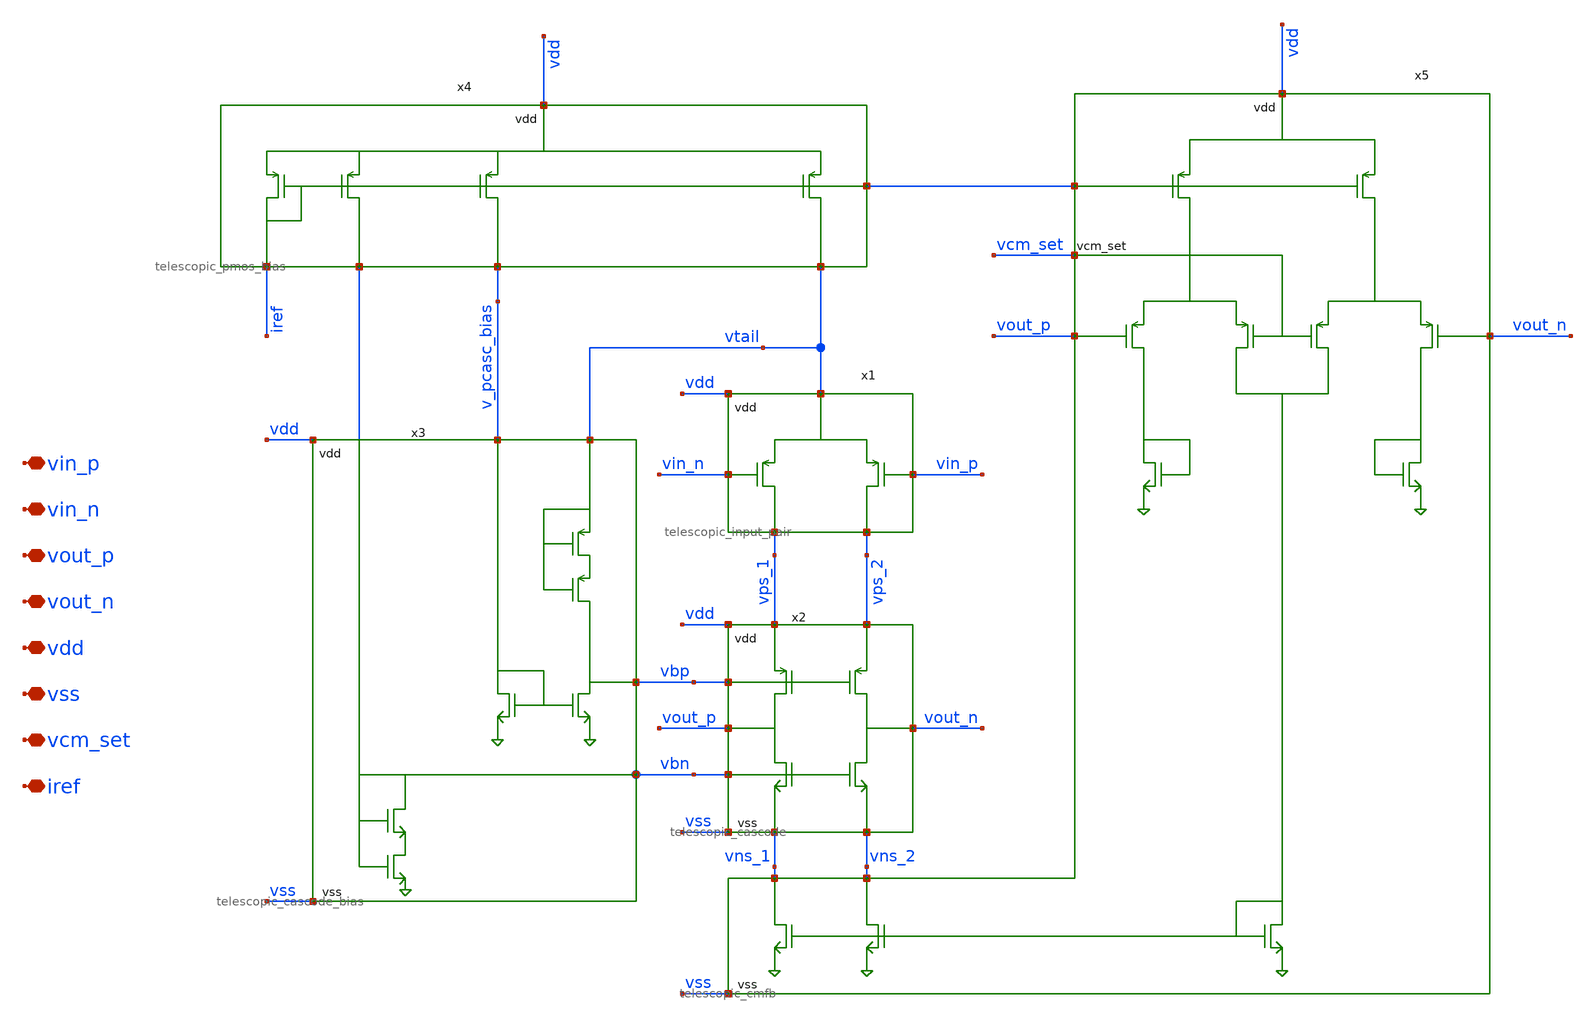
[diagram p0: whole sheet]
** sch_path: xschem/archive/rrl/telescopic.sch
**.subckt telescopic vin_p vin_n vout_p vout_n vdd vss vcm_set iref
*.iopin vin_p
*.iopin vin_n
*.iopin vout_p
*.iopin vout_n
*.iopin vdd
*.iopin vss
*.iopin vcm_set
*.iopin iref
x1 vtail vdd vin_n vin_p vps_1 vps_2 telescopic_input_pair
x2 vdd vss vps_1 vps_2 vns_1 vns_2 vout_p vout_n vbp vbn telescopic_cascode
x3 vbn v_pcasc_bias vtail vbp vss vdd telescopic_cascode_bias
x4 vdd vbn v_pcasc_bias vtail iref telescopic_pmos_bias
x5 vns_1 vns_2 vout_p vout_n iref vdd vss vcm_set telescopic_cmfb
**.ends
.end
